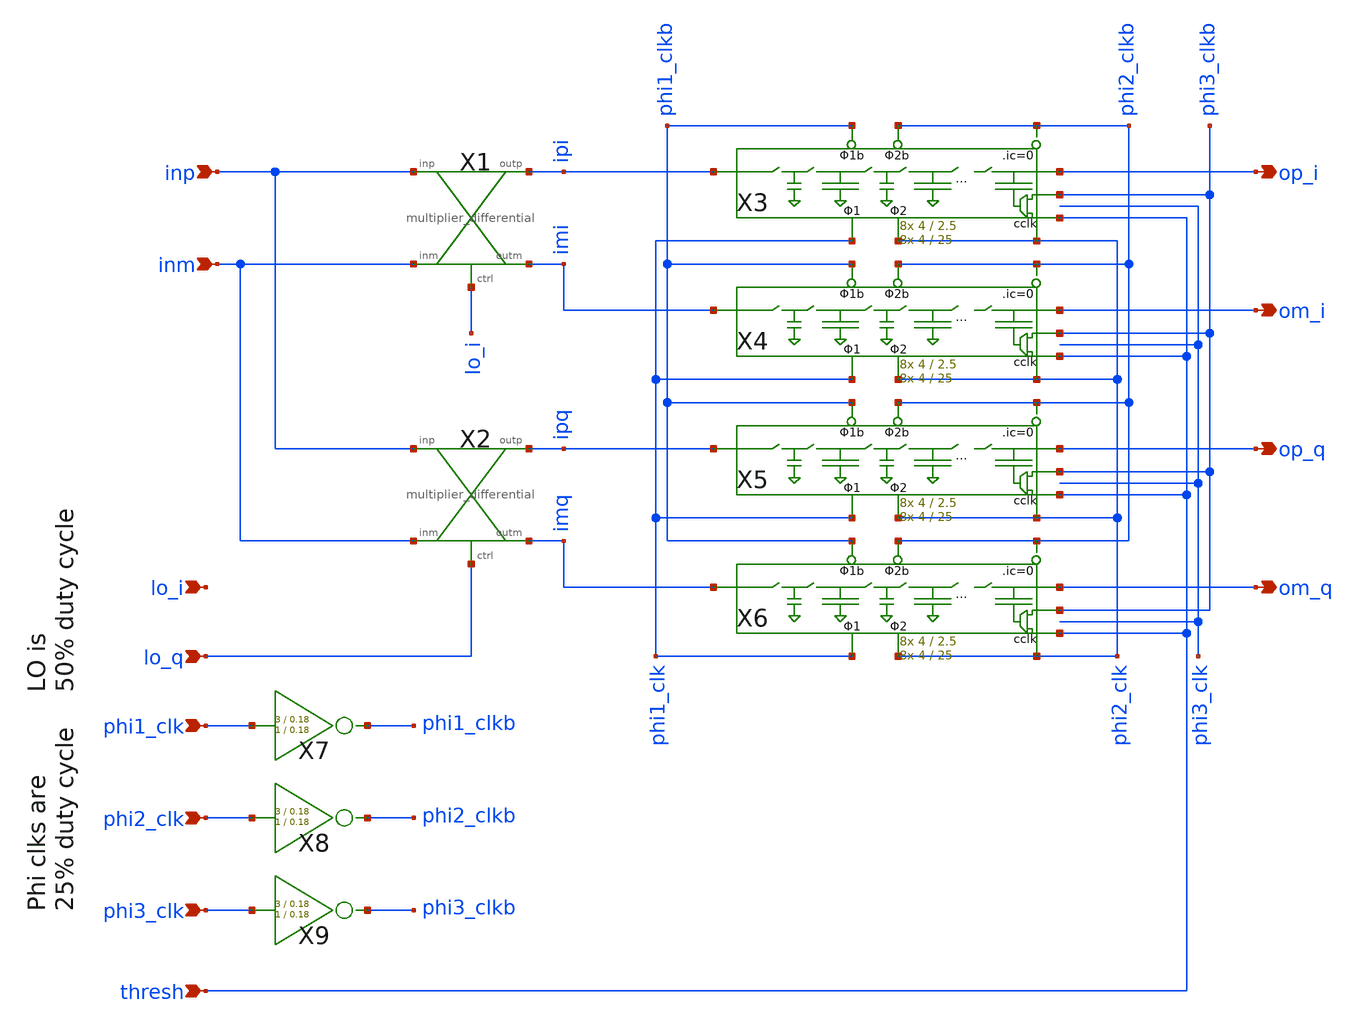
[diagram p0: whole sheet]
** sch_path: xschem/wavelet_channel/wavelet_iq_thresh.sch
**.subckt wavelet_iq_thresh inp inm phi1_clk phi2_clk lo_q lo_i op_i om_i op_q om_q thresh phi3_clk
*.ipin inp
*.ipin inm
*.ipin phi1_clk
*.ipin phi2_clk
*.ipin lo_q
*.ipin lo_i
*.opin op_i
*.opin om_i
*.opin op_q
*.opin om_q
*.ipin thresh
*.ipin phi3_clk
X8 phi2_clk phi2_clkb inv Wpmos=3 Lpmos=0.18 Wnmos=1 Lnmos=0.18
X1 inp ipi inm lo_i imi multiplier_differential
X2 inp ipq inm lo_q imq multiplier_differential
X7 phi1_clk phi1_clkb inv Wpmos=3 Lpmos=0.18 Wnmos=1 Lnmos=0.18
X9 phi3_clk phi3_clkb inv Wpmos=3 Lpmos=0.18 Wnmos=1 Lnmos=0.18
X3 ipi op_i phi1_clk phi1_clkb phi2_clk phi2_clkb phi2_clk phi3_clkb thresh phi2_clkb
+ 16switchcaps_2phi_thresh Wcap1=4 Lcap1=2.5 Wcap2=4 Lcap2=25
X4 imi om_i phi1_clk phi1_clkb phi2_clk phi2_clkb phi2_clk phi3_clkb thresh phi2_clkb
+ 16switchcaps_2phi_thresh Wcap1=4 Lcap1=2.5 Wcap2=4 Lcap2=25
X5 ipq op_q phi1_clk phi1_clkb phi2_clk phi2_clkb phi2_clk phi3_clkb thresh phi2_clkb
+ 16switchcaps_2phi_thresh Wcap1=4 Lcap1=2.5 Wcap2=4 Lcap2=25
X6 imq om_q phi1_clk phi1_clkb phi2_clk phi2_clkb phi2_clk phi3_clkb thresh phi2_clkb
+ 16switchcaps_2phi_thresh Wcap1=4 Lcap1=2.5 Wcap2=4 Lcap2=25
**.ends

* expanding   symbol:  inv/inv.sym # of pins=2
** sym_path: xschem/inv/inv.sym
** sch_path: xschem/inv/inv.sch
.subckt inv in out  Wpmos=3 Lpmos=0.18 Wnmos=1 Lnmos=0.18
*.ipin in
*.iopin out
XM1 out in GND GND sky130_fd_pr__nfet_01v8 L=Lnmos W=Wnmos nf=1 ad='int((nf+1)/2) * W/nf * 0.29' as='int((nf+2)/2) * W/nf * 0.29'
+ pd='2*int((nf+1)/2) * (W/nf + 0.29)' ps='2*int((nf+2)/2) * (W/nf + 0.29)' nrd='0.29 / W' nrs='0.29 / W'
+ sa=0 sb=0 sd=0 mult=1 m=1
XM2 out in VDD VDD sky130_fd_pr__pfet_01v8 L=Lpmos W=Wpmos nf=1 ad='int((nf+1)/2) * W/nf * 0.29' as='int((nf+2)/2) * W/nf * 0.29'
+ pd='2*int((nf+1)/2) * (W/nf + 0.29)' ps='2*int((nf+2)/2) * (W/nf + 0.29)' nrd='0.29 / W' nrs='0.29 / W'
+ sa=0 sb=0 sd=0 mult=1 m=1
.ends


* expanding   symbol:  mux/multiplier_differential.sym # of pins=5
** sym_path: xschem/mux/multiplier_differential.sym
** sch_path: xschem/mux/multiplier_differential.sch
.subckt multiplier_differential inp outp inm ctrl outm
*.ipin inp
*.ipin inm
*.opin outp
*.opin outm
*.ipin ctrl
X1 inp outp inm ctrl mux2-1
X2 inm outm inp ctrl mux2-1
.ends


* expanding   symbol:  Switched_Caps/16switchcaps_2phi_thresh.sym # of pins=10
** sym_path: xschem/Switched_Caps/16switchcaps_2phi_thresh.sym
** sch_path: xschem/Switched_Caps/16switchcaps_2phi_thresh.sch
.subckt 16switchcaps_2phi_thresh in out phi1_clk phi1_clkb phi2_clk phi2_clkb cclk thresh1 thresh2
+ cclkb  Wcap1=4 Lcap1=2.5 Wcap2=4 Lcap2=25
*.iopin in
*.iopin out
*.ipin phi2_clkb
*.ipin phi1_clkb
*.ipin phi2_clk
*.ipin phi1_clk
*.ipin thresh1
*.ipin cclk
*.ipin thresh2
*.ipin cclkb
X1 in c2 phi2_clk phi1_clk phi1_clkb phi2_clkb 2switchcaps Wcap1=Wcap1 Lcap1=Lcap1 Wcap2=4 Lcap2=25
X2 c2 c4 phi2_clk phi1_clk phi1_clkb phi2_clkb 2switchcaps Wcap1=Wcap1 Lcap1=Lcap1 Wcap2=4 Lcap2=25
X3 c4 c6 phi2_clk phi1_clk phi1_clkb phi2_clkb 2switchcaps Wcap1=Wcap1 Lcap1=Lcap1 Wcap2=4 Lcap2=25
X4 c6 c8 phi2_clk phi1_clk phi1_clkb phi2_clkb 2switchcaps Wcap1=Wcap1 Lcap1=Lcap1 Wcap2=4 Lcap2=25
X5 c8 c10 phi2_clk phi1_clk phi1_clkb phi2_clkb 2switchcaps Wcap1=Wcap1 Lcap1=Lcap1 Wcap2=4 Lcap2=25
X6 c10 c12 phi2_clk phi1_clk phi1_clkb phi2_clkb 2switchcaps Wcap1=Wcap1 Lcap1=Lcap1 Wcap2=4
+ Lcap2=25
X7 c12 c14 phi2_clk phi1_clk phi1_clkb phi2_clkb 2switchcaps Wcap1=Wcap1 Lcap1=Lcap1 Wcap2=4
+ Lcap2=25
X8 c14 out phi2_clk phi1_clk phi1_clkb phi2_clkb thresh2 cclk thresh1 cclkb 2switchcaps_thresh
+ Wcap=20 Lcap=20
.ends


* expanding   symbol:  mux/mux2-1.sym # of pins=4
** sym_path: xschem/mux/mux2-1.sym
** sch_path: xschem/mux/mux2-1.sch
.subckt mux2-1 in1 out in2 ctrl
*.ipin in1
*.ipin ctrl
*.ipin in2
*.iopin out
X1 in1 out net1 ctrl transmission_gate Wpmos=3 Lpmos=0.18 Wnmos=1 Lnmos=0.18
X2 in2 out ctrl net1 transmission_gate Wpmos=3 Lpmos=0.18 Wnmos=1 Lnmos=0.18
X4 ctrl net1 inv Wpmos=3 Lpmos=0.18 Wnmos=1 Lnmos=0.18
.ends


* expanding   symbol:  Switched_Caps/2switchcaps.sym # of pins=6
** sym_path: xschem/Switched_Caps/2switchcaps.sym
** sch_path: xschem/Switched_Caps/2switchcaps.sch
.subckt 2switchcaps in out phi2_clk_n phi1_clk_n phi1_clk_p phi2_clk_p  Wcap1=4 Lcap1=2.5 Wcap2=4
+ Lcap2=25
*.iopin out
*.iopin in
*.ipin phi1_clk_n
*.ipin phi1_clk_p
*.ipin phi2_clk_p
*.ipin phi2_clk_n
XC1 c1 GND sky130_fd_pr__cap_mim_m3_1 W=Wcap L=Lcap MF=1 m=1
XC2 out GND sky130_fd_pr__cap_mim_m3_1 W=Wcap L=Lcap MF=1 m=1
**** begin user architecture code

.ic v(c1)=0 v(out)=0

**** end user architecture code
X1 in c1 phi1_clk_p phi1_clk_n transmission_gate Wpmos=3 Lpmos=0.18 Wnmos=1 Lnmos=0.18
X2 c1 out phi2_clk_p phi2_clk_n transmission_gate Wpmos=3 Lpmos=0.18 Wnmos=1 Lnmos=0.18
.ends


* expanding   symbol:  Switched_Caps/2switchcaps_thresh.sym # of pins=10
** sym_path: xschem/Switched_Caps/2switchcaps_thresh.sym
** sch_path: xschem/Switched_Caps/2switchcaps_thresh.sch
.subckt 2switchcaps_thresh in out phi2_clk_n phi1_clk_n phi1_clk_p phi2_clk_p thresh2 cclk thresh1
+ cclkb  Wcap=20 Lcap=20
*.iopin out
*.iopin in
*.ipin phi1_clk_n
*.ipin phi1_clk_p
*.ipin phi2_clk_p
*.ipin phi2_clk_n
*.ipin thresh1
*.ipin cclk
*.ipin thresh2
*.ipin cclkb
XC1 c1 GND sky130_fd_pr__cap_mim_m3_1 W=Wcap1 L=Lcap1 MF=1 m=1
XC2 out c2b sky130_fd_pr__cap_mim_m3_1 W=Wcap2 L=Lcap2 MF=1 m=1
**** begin user architecture code


*init cap top and bottom plates at 0V:
.ic v(c1)=0 v(out)=0
*c2 will settle at thresh1
*.ic v(xc1.a)=0 v(xc1.b1)=0 v(xc2.a)=0 v(xc2.b1)=0


**** end user architecture code
X1 in c1 phi1_clk_p phi1_clk_n transmission_gate Wpmos=0.42 Lpmos=0.18 Wnmos=0.42 Lnmos=0.18
X2 c1 out phi2_clk_p phi2_clk_n transmission_gate Wpmos=0.42 Lpmos=0.18 Wnmos=0.42 Lnmos=0.18
x3 thresh2 thresh1 cclk cclkb c2b analogMux
.ends


* expanding   symbol:  transmission_gate/transmission_gate.sym # of pins=4
** sym_path: xschem/transmission_gate/transmission_gate.sym
** sch_path: xschem/transmission_gate/transmission_gate.sch
.subckt transmission_gate in out ctrl_ ctrl  Wpmos=1 Lpmos=0.18 Wnmos=1 Lnmos=0.18
*.iopin in
*.iopin out
*.ipin ctrl_
*.ipin ctrl
XM1 in ctrl out GND sky130_fd_pr__nfet_01v8 L=Lnmos W=Wnmos nf=1 ad='int((nf+1)/2) * W/nf * 0.29' as='int((nf+2)/2) * W/nf * 0.29'
+ pd='2*int((nf+1)/2) * (W/nf + 0.29)' ps='2*int((nf+2)/2) * (W/nf + 0.29)' nrd='0.29 / W' nrs='0.29 / W'
+ sa=0 sb=0 sd=0 mult=1 m=1
XM2 out ctrl_ in VDD sky130_fd_pr__pfet_01v8 L=Lpmos W=Wpmos nf=1 ad='int((nf+1)/2) * W/nf * 0.29' as='int((nf+2)/2) * W/nf * 0.29'
+ pd='2*int((nf+1)/2) * (W/nf + 0.29)' ps='2*int((nf+2)/2) * (W/nf + 0.29)' nrd='0.29 / W' nrs='0.29 / W'
+ sa=0 sb=0 sd=0 mult=1 m=1
.ends


* expanding   symbol:  comparator/analogMux.sym # of pins=5
** sym_path: xschem/comparator/analogMux.sym
** sch_path: xschem/comparator/analogMux.sch
.subckt analogMux Vref2 Vref1 C Cbar out
*.ipin Vref1
*.opin out
*.ipin Vref2
*.ipin C
*.ipin Cbar
XM1 Vref1 C out GND sky130_fd_pr__nfet_01v8 L=1 W=4 nf=1 ad='int((nf+1)/2) * W/nf * 0.29' as='int((nf+2)/2) * W/nf * 0.29'
+ pd='2*int((nf+1)/2) * (W/nf + 0.29)' ps='2*int((nf+2)/2) * (W/nf + 0.29)' nrd='0.29 / W' nrs='0.29 / W'
+ sa=0 sb=0 sd=0 mult=1 m=1
XM2 Vref1 Cbar out VDD sky130_fd_pr__pfet_01v8 L=1 W=8 nf=1 ad='int((nf+1)/2) * W/nf * 0.29' as='int((nf+2)/2) * W/nf * 0.29'
+ pd='2*int((nf+1)/2) * (W/nf + 0.29)' ps='2*int((nf+2)/2) * (W/nf + 0.29)' nrd='0.29 / W' nrs='0.29 / W'
+ sa=0 sb=0 sd=0 mult=1 m=1
XM3 out Cbar Vref2 GND sky130_fd_pr__nfet_01v8 L=1 W=4 nf=1 ad='int((nf+1)/2) * W/nf * 0.29' as='int((nf+2)/2) * W/nf * 0.29'
+ pd='2*int((nf+1)/2) * (W/nf + 0.29)' ps='2*int((nf+2)/2) * (W/nf + 0.29)' nrd='0.29 / W' nrs='0.29 / W'
+ sa=0 sb=0 sd=0 mult=1 m=1
XM4 out C Vref2 VDD sky130_fd_pr__pfet_01v8 L=1 W=8 nf=1 ad='int((nf+1)/2) * W/nf * 0.29' as='int((nf+2)/2) * W/nf * 0.29'
+ pd='2*int((nf+1)/2) * (W/nf + 0.29)' ps='2*int((nf+2)/2) * (W/nf + 0.29)' nrd='0.29 / W' nrs='0.29 / W'
+ sa=0 sb=0 sd=0 mult=1 m=1
.ends

.GLOBAL VDD
.GLOBAL GND
.end
